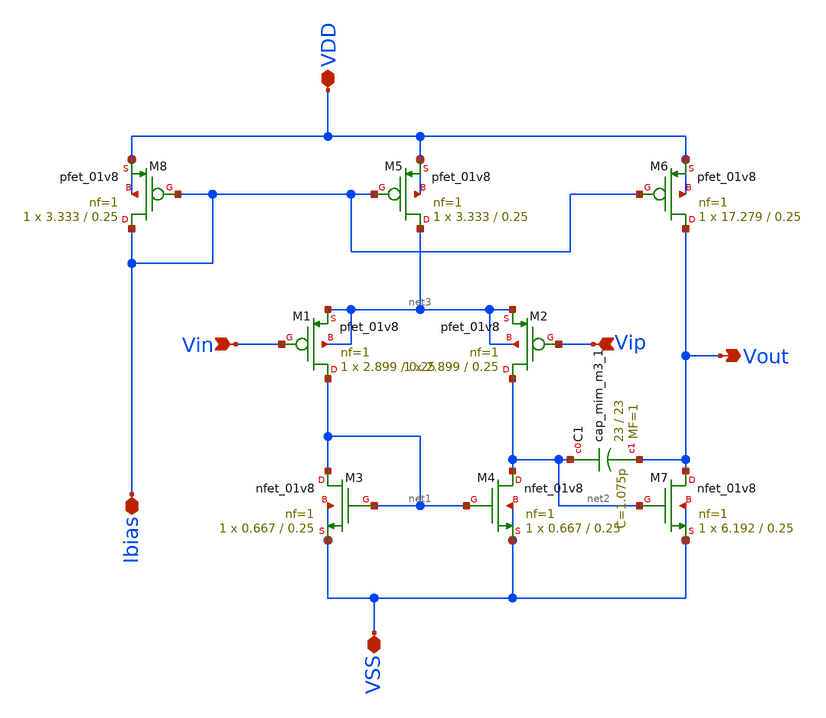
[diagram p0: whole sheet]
** sch_path: xschem/Ota_esq.sch
**.subckt Ota_esq Vin Vip VDD VSS Ibias Vout
*.ipin Vin
*.ipin Vip
*.iopin VDD
*.iopin VSS
*.iopin Ibias
*.opin Vout
XM1 net1 Vin net3 net3 sky130_fd_pr__pfet_01v8 L=0.25 W=2.899 nf=1 ad='int((nf+1)/2) * W/nf * 0.29' as='int((nf+2)/2) * W/nf * 0.29'
+ pd='2*int((nf+1)/2) * (W/nf + 0.29)' ps='2*int((nf+2)/2) * (W/nf + 0.29)' nrd='0.29 / W' nrs='0.29 / W'
+ sa=0 sb=0 sd=0 mult=1 m=1
XM2 net2 Vip net3 net3 sky130_fd_pr__pfet_01v8 L=0.25 W=2.899 nf=1 ad='int((nf+1)/2) * W/nf * 0.29' as='int((nf+2)/2) * W/nf * 0.29'
+ pd='2*int((nf+1)/2) * (W/nf + 0.29)' ps='2*int((nf+2)/2) * (W/nf + 0.29)' nrd='0.29 / W' nrs='0.29 / W'
+ sa=0 sb=0 sd=0 mult=1 m=1
XM3 net1 net1 VSS VSS sky130_fd_pr__nfet_01v8 L=0.25 W=0.667 nf=1 ad='int((nf+1)/2) * W/nf * 0.29' as='int((nf+2)/2) * W/nf * 0.29'
+ pd='2*int((nf+1)/2) * (W/nf + 0.29)' ps='2*int((nf+2)/2) * (W/nf + 0.29)' nrd='0.29 / W' nrs='0.29 / W'
+ sa=0 sb=0 sd=0 mult=1 m=1
XM4 net2 net1 VSS VSS sky130_fd_pr__nfet_01v8 L=0.25 W=0.667 nf=1 ad='int((nf+1)/2) * W/nf * 0.29' as='int((nf+2)/2) * W/nf * 0.29'
+ pd='2*int((nf+1)/2) * (W/nf + 0.29)' ps='2*int((nf+2)/2) * (W/nf + 0.29)' nrd='0.29 / W' nrs='0.29 / W'
+ sa=0 sb=0 sd=0 mult=1 m=1
XM5 net3 Ibias VDD VDD sky130_fd_pr__pfet_01v8 L=0.25 W=3.333 nf=1 ad='int((nf+1)/2) * W/nf * 0.29' as='int((nf+2)/2) * W/nf * 0.29'
+ pd='2*int((nf+1)/2) * (W/nf + 0.29)' ps='2*int((nf+2)/2) * (W/nf + 0.29)' nrd='0.29 / W' nrs='0.29 / W'
+ sa=0 sb=0 sd=0 mult=1 m=1
XM8 Ibias Ibias VDD VDD sky130_fd_pr__pfet_01v8 L=0.25 W=3.333 nf=1 ad='int((nf+1)/2) * W/nf * 0.29'
+ as='int((nf+2)/2) * W/nf * 0.29' pd='2*int((nf+1)/2) * (W/nf + 0.29)' ps='2*int((nf+2)/2) * (W/nf + 0.29)'
+ nrd='0.29 / W' nrs='0.29 / W' sa=0 sb=0 sd=0 mult=1 m=1
XM6 Vout Ibias VDD VDD sky130_fd_pr__pfet_01v8 L=0.25 W=17.279 nf=1 ad='int((nf+1)/2) * W/nf * 0.29'
+ as='int((nf+2)/2) * W/nf * 0.29' pd='2*int((nf+1)/2) * (W/nf + 0.29)' ps='2*int((nf+2)/2) * (W/nf + 0.29)'
+ nrd='0.29 / W' nrs='0.29 / W' sa=0 sb=0 sd=0 mult=1 m=1
XM7 Vout net2 VSS VSS sky130_fd_pr__nfet_01v8 L=0.25 W=6.192 nf=1 ad='int((nf+1)/2) * W/nf * 0.29' as='int((nf+2)/2) * W/nf * 0.29'
+ pd='2*int((nf+1)/2) * (W/nf + 0.29)' ps='2*int((nf+2)/2) * (W/nf + 0.29)' nrd='0.29 / W' nrs='0.29 / W'
+ sa=0 sb=0 sd=0 mult=1 m=1
XC1 net2 Vout sky130_fd_pr__cap_mim_m3_1 W=23 L=23 MF=1 m=1
**.ends
.end
